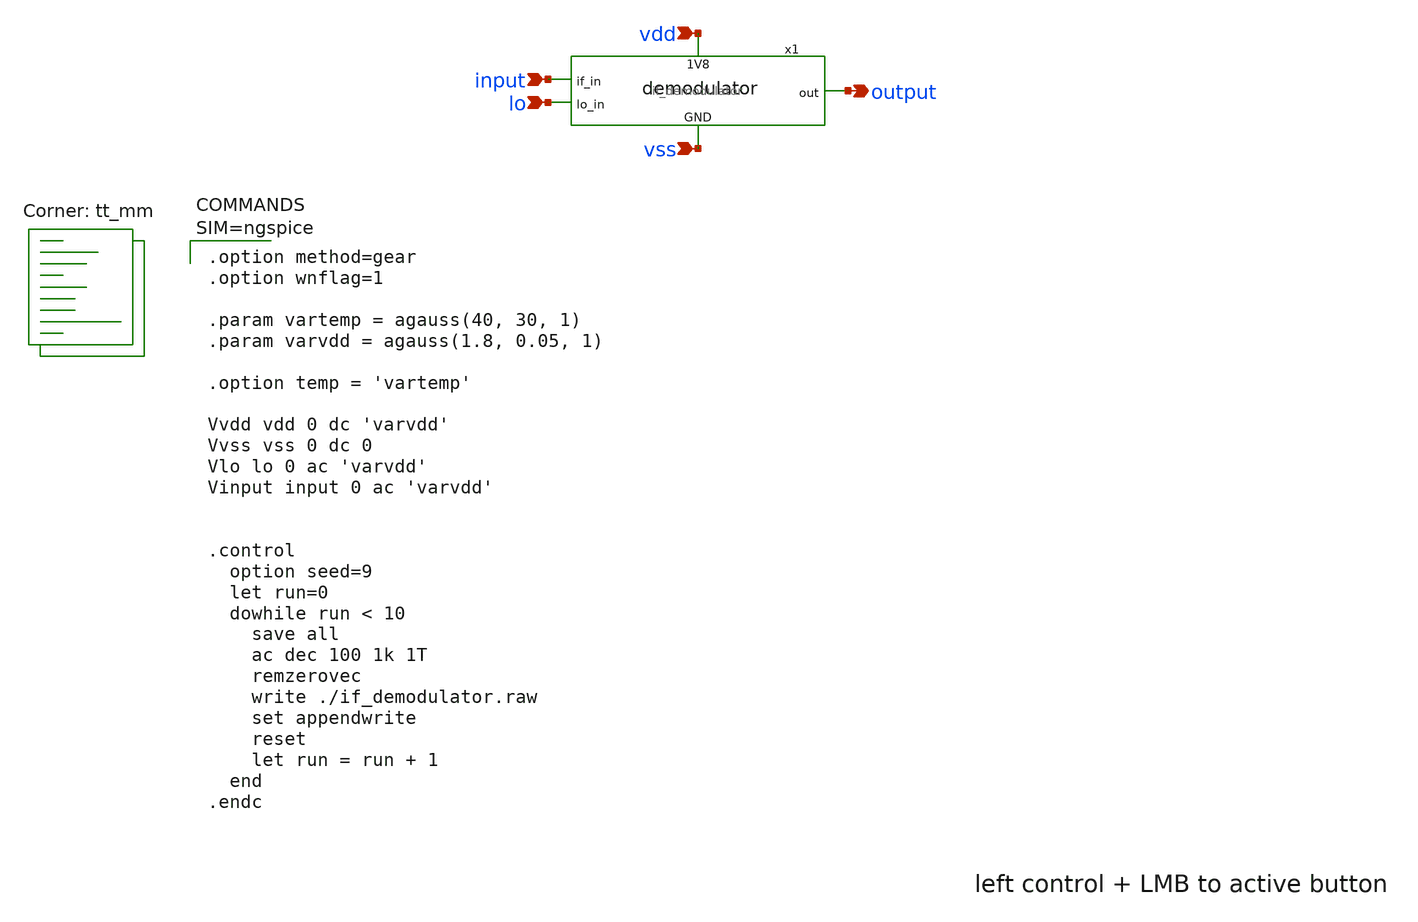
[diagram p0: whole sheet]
** sch_path: tests/if_demodulator.sch
**.subckt if_demodulator input vdd vss lo output
*.ipin input
*.ipin vdd
*.ipin vss
*.ipin lo
*.opin output
x1 input lo vdd output vss if_demodulator
**** begin user architecture code
.lib $::SKYWATER_MODELS/sky130.lib.spice tt_mm


.option method=gear
.option wnflag=1

.param vartemp = agauss(40, 30, 1)
.param varvdd = agauss(1.8, 0.05, 1)

.option temp = 'vartemp'

Vvdd vdd 0 dc 'varvdd'
Vvss vss 0 dc 0
Vlo lo 0 ac 'varvdd'
Vinput input 0 ac 'varvdd'


.control
  option seed=9
  let run=0
  dowhile run < 10
    save all
    ac dec 100 1k 1T
    remzerovec
    write ./if_demodulator.raw
    set appendwrite
    reset
    let run = run + 1
  end
.endc


**** end user architecture code
**.ends

* expanding   symbol:  ./if_demodulator.sym # of pins=5
** sym_path: schematic/if_demodulator.sym
** sch_path: schematic/if_demodulator.sch
.subckt if_demodulator if_in lo_in 1V8 out GND
*.ipin if_in
*.opin out
*.ipin GND
*.ipin 1V8
*.ipin lo_in
* noconn 1V8
* noconn GND
* noconn lo_in
R1 out if_in 0 m=1
.ends

.end
